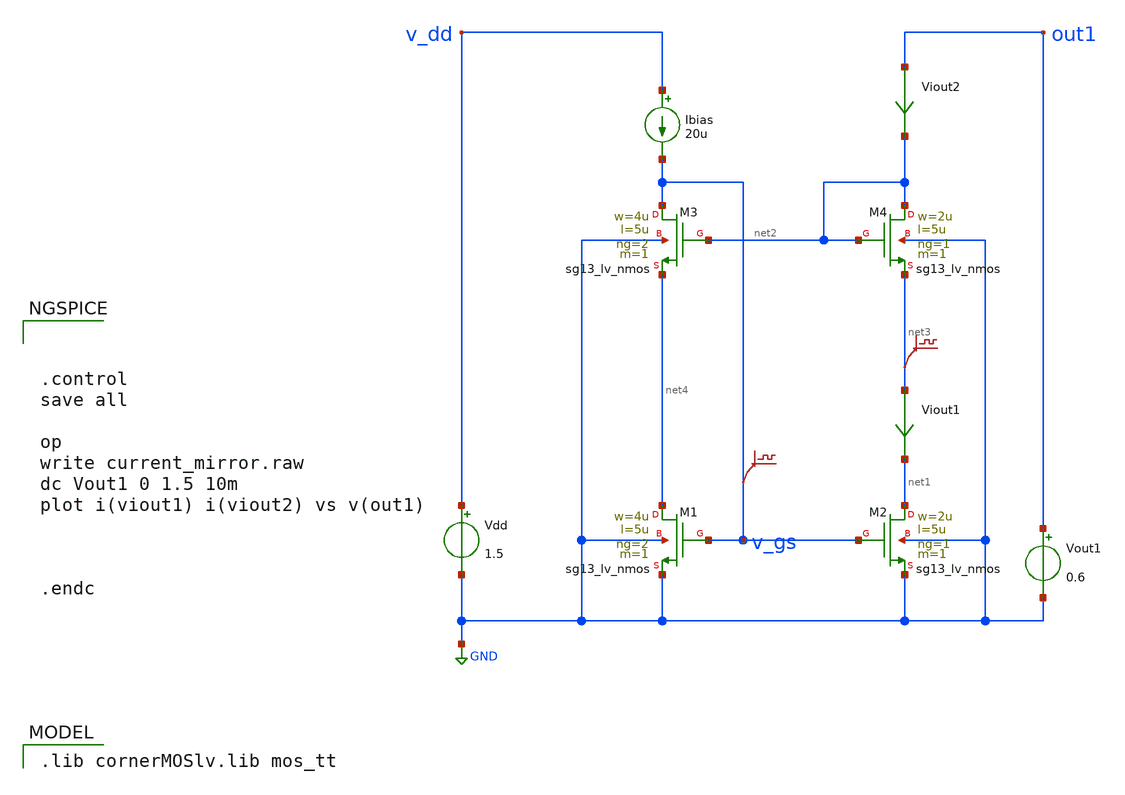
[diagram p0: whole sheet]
** sch_path: Designs/current_mirror/modified_wilsons_current_mirror.sch
* (c) 2025 Thesis_HP, Apache-2.0 license
**.subckt modified_wilsons_current_mirror
Vdd v_dd GND 1.5
XM1 net4 v_gs GND GND sg13_lv_nmos w=4u l=5u ng=2 m=1 mm_ok=1
Ibias v_dd v_gs 20u
XM2 net1 v_gs GND GND sg13_lv_nmos w=2u l=5u ng=1 m=1 mm_ok=1
Vout1 out1 GND 0.6
.save v(net3)
.save v(v_gs)
Viout1 net3 net1 0
.save i(viout1)
XM3 v_gs net2 net4 GND sg13_lv_nmos w=4u l=5u ng=2 m=1 mm_ok=1
XM4 net2 net2 net3 GND sg13_lv_nmos w=2u l=5u ng=1 m=1 mm_ok=1
Viout2 out1 net2 0
.save i(viout2)
**** begin user architecture code
 .lib cornerMOSlv.lib mos_tt




.control
save all

op
write current_mirror.raw
dc Vout1 0 1.5 10m
plot i(viout1) i(viout2) vs v(out1)



.endc


**** end user architecture code
**.ends
.GLOBAL GND
.end
